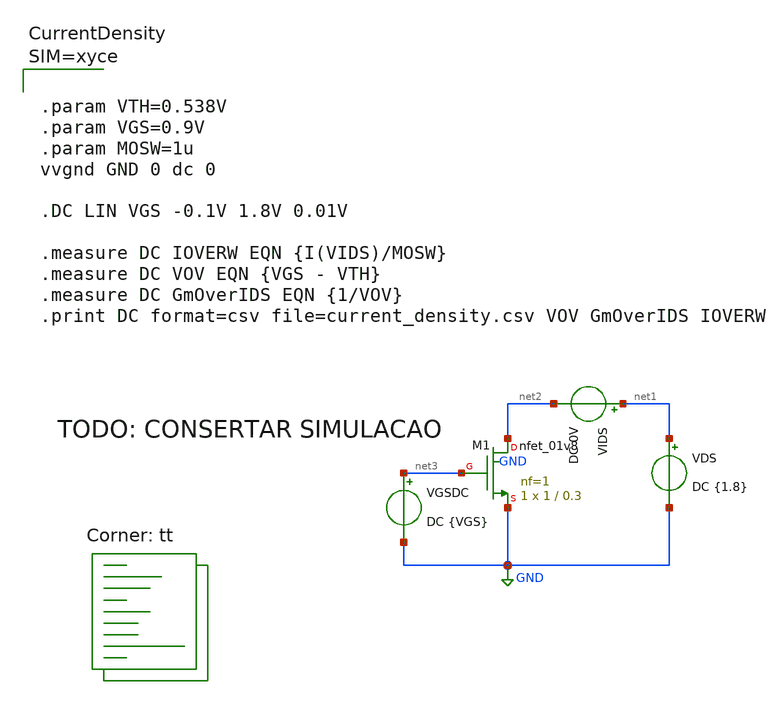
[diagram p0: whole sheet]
** sch_path: sky130/xschem/current-density.sch
**.subckt current-density
XM1 net2 net3 GND GND sky130_fd_pr__nfet_01v8 L=0.3 W=1 nf=1 ad='int((nf+1)/2) * W/nf * 0.29' as='int((nf+2)/2) * W/nf * 0.29'
+ pd='2*int((nf+1)/2) * (W/nf + 0.29)' ps='2*int((nf+2)/2) * (W/nf + 0.29)' nrd='0.29 / W' nrs='0.29 / W'
+ sa=0 sb=0 sd=0 mult=1 m=1
VDS net1 GND DC {1.8}
VGSDC net3 GND DC {VGS}
VIDS net1 net2 DC 0V
**** begin user architecture code
.lib $::SKYWATER_MODELS/sky130.lib.spice tt



**** end user architecture code
**.ends
.GLOBAL GND
.end
